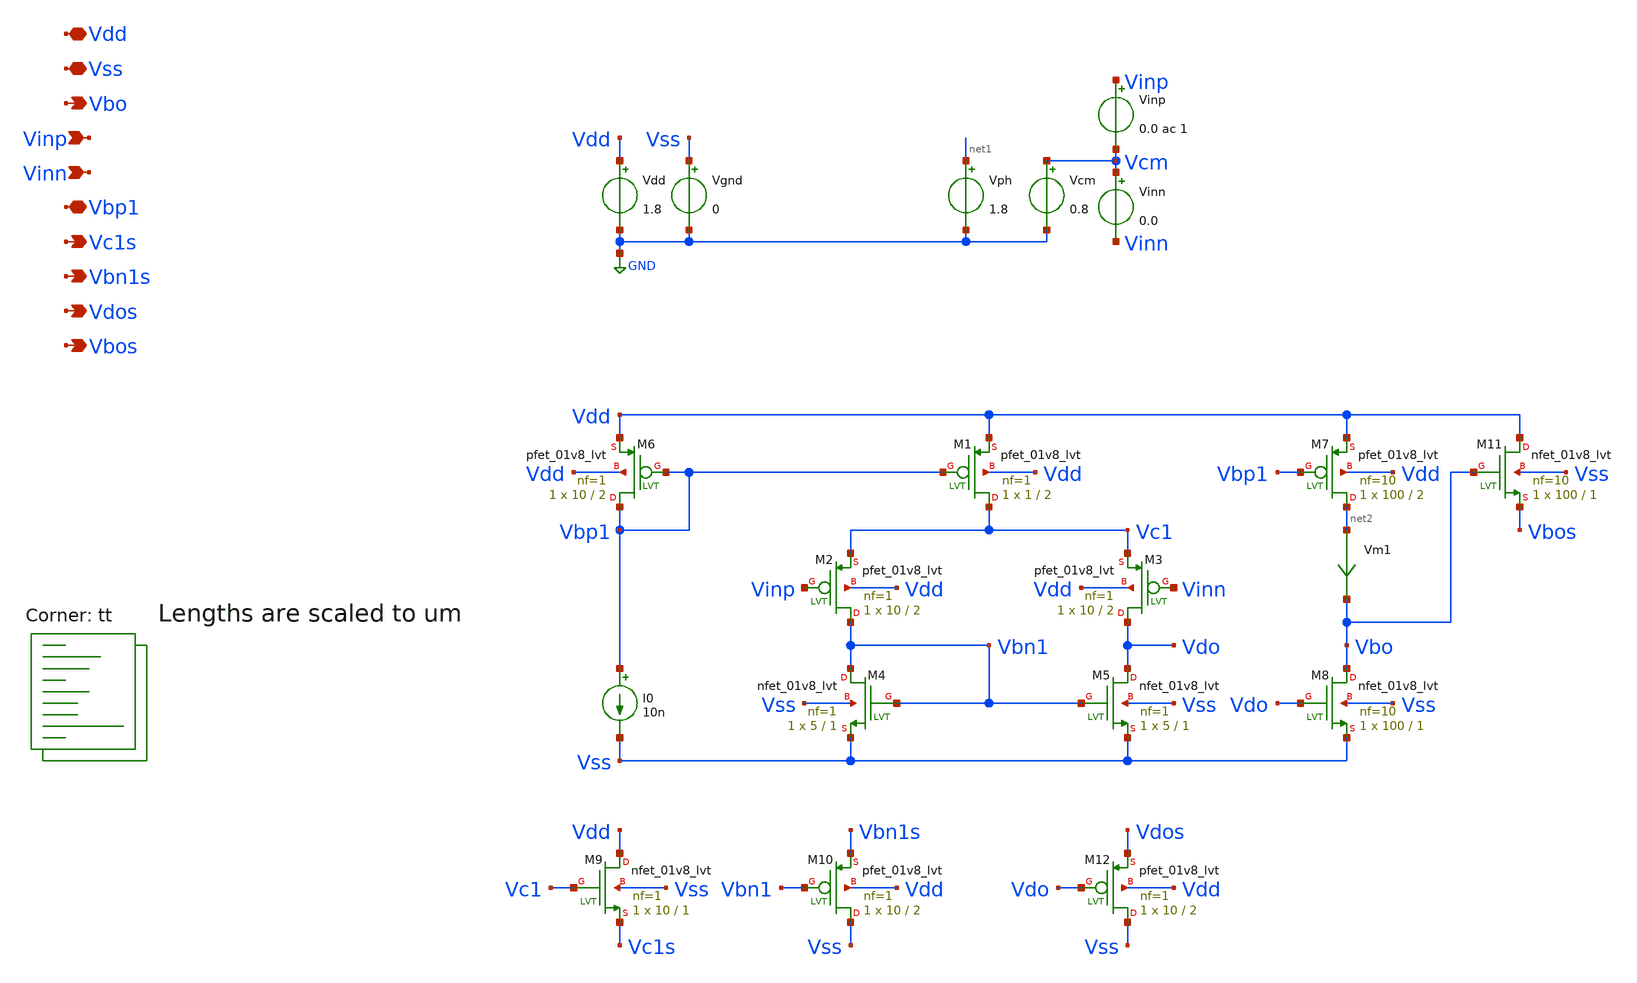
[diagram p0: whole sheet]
** sch_path: ic/CntDiffAmp/Schematic/CntDiffAmp0.sch
**.subckt CntDiffAmp0 Vinp Vbo Vinn Vdd Vss Vbp1 Vc1s Vbn1s Vdos Vbos
*.ipin Vinp
*.opin Vbo
*.ipin Vinn
*.iopin Vdd
*.iopin Vss
*.iopin Vbp1
*.opin Vc1s
*.opin Vbn1s
*.opin Vdos
*.opin Vbos
XM5 Vdo Vbn1 Vss Vss sky130_fd_pr__nfet_01v8_lvt L=1 W=5 nf=1 ad='int((nf+1)/2) * W/nf * 0.29' as='int((nf+2)/2) * W/nf * 0.29'
+ pd='2*int((nf+1)/2) * (W/nf + 0.29)' ps='2*int((nf+2)/2) * (W/nf + 0.29)' nrd='0.29 / W' nrs='0.29 / W'
+ sa=0 sb=0 sd=0 mult=1 m=1
XM4 Vbn1 Vbn1 Vss Vss sky130_fd_pr__nfet_01v8_lvt L=1 W=5 nf=1 ad='int((nf+1)/2) * W/nf * 0.29' as='int((nf+2)/2) * W/nf * 0.29'
+ pd='2*int((nf+1)/2) * (W/nf + 0.29)' ps='2*int((nf+2)/2) * (W/nf + 0.29)' nrd='0.29 / W' nrs='0.29 / W'
+ sa=0 sb=0 sd=0 mult=1 m=1
I0 Vbp1 Vss 10n
Vdd Vdd GND 1.8
Vgnd Vss GND 0
Vinp Vinp Vcm 0.0 ac 1
Vinn Vcm Vinn 0.0
Vph net1 GND 1.8
Vcm Vcm GND 0.8
XM1 Vc1 Vbp1 Vdd Vdd sky130_fd_pr__pfet_01v8_lvt L=2 W=1 nf=1 ad='int((nf+1)/2) * W/nf * 0.29' as='int((nf+2)/2) * W/nf * 0.29'
+ pd='2*int((nf+1)/2) * (W/nf + 0.29)' ps='2*int((nf+2)/2) * (W/nf + 0.29)' nrd='0.29 / W' nrs='0.29 / W'
+ sa=0 sb=0 sd=0 mult=1 m=1
XM6 Vbp1 Vbp1 Vdd Vdd sky130_fd_pr__pfet_01v8_lvt L=2 W=10 nf=1 ad='int((nf+1)/2) * W/nf * 0.29' as='int((nf+2)/2) * W/nf * 0.29'
+ pd='2*int((nf+1)/2) * (W/nf + 0.29)' ps='2*int((nf+2)/2) * (W/nf + 0.29)' nrd='0.29 / W' nrs='0.29 / W'
+ sa=0 sb=0 sd=0 mult=1 m=1
XM2 Vbn1 Vinp Vc1 Vdd sky130_fd_pr__pfet_01v8_lvt L=2 W=10 nf=1 ad='int((nf+1)/2) * W/nf * 0.29' as='int((nf+2)/2) * W/nf * 0.29'
+ pd='2*int((nf+1)/2) * (W/nf + 0.29)' ps='2*int((nf+2)/2) * (W/nf + 0.29)' nrd='0.29 / W' nrs='0.29 / W'
+ sa=0 sb=0 sd=0 mult=1 m=1
XM3 Vdo Vinn Vc1 Vdd sky130_fd_pr__pfet_01v8_lvt L=2 W=10 nf=1 ad='int((nf+1)/2) * W/nf * 0.29' as='int((nf+2)/2) * W/nf * 0.29'
+ pd='2*int((nf+1)/2) * (W/nf + 0.29)' ps='2*int((nf+2)/2) * (W/nf + 0.29)' nrd='0.29 / W' nrs='0.29 / W'
+ sa=0 sb=0 sd=0 mult=1 m=1
XM7 net2 Vbp1 Vdd Vdd sky130_fd_pr__pfet_01v8_lvt L=2 W=100 nf=10 ad='int((nf+1)/2) * W/nf * 0.29' as='int((nf+2)/2) * W/nf * 0.29'
+ pd='2*int((nf+1)/2) * (W/nf + 0.29)' ps='2*int((nf+2)/2) * (W/nf + 0.29)' nrd='0.29 / W' nrs='0.29 / W'
+ sa=0 sb=0 sd=0 mult=1 m=1
XM8 Vbo Vdo Vss Vss sky130_fd_pr__nfet_01v8_lvt L=1 W=100 nf=10 ad='int((nf+1)/2) * W/nf * 0.29' as='int((nf+2)/2) * W/nf * 0.29'
+ pd='2*int((nf+1)/2) * (W/nf + 0.29)' ps='2*int((nf+2)/2) * (W/nf + 0.29)' nrd='0.29 / W' nrs='0.29 / W'
+ sa=0 sb=0 sd=0 mult=1 m=1
Vm1 net2 Vbo 0
.save i(vm1)
XM9 Vdd Vc1 Vc1s Vss sky130_fd_pr__nfet_01v8_lvt L=1 W=10 nf=1 ad='int((nf+1)/2) * W/nf * 0.29' as='int((nf+2)/2) * W/nf * 0.29'
+ pd='2*int((nf+1)/2) * (W/nf + 0.29)' ps='2*int((nf+2)/2) * (W/nf + 0.29)' nrd='0.29 / W' nrs='0.29 / W'
+ sa=0 sb=0 sd=0 mult=1 m=1
XM10 Vss Vbn1 Vbn1s Vdd sky130_fd_pr__pfet_01v8_lvt L=2 W=10 nf=1 ad='int((nf+1)/2) * W/nf * 0.29' as='int((nf+2)/2) * W/nf * 0.29'
+ pd='2*int((nf+1)/2) * (W/nf + 0.29)' ps='2*int((nf+2)/2) * (W/nf + 0.29)' nrd='0.29 / W' nrs='0.29 / W'
+ sa=0 sb=0 sd=0 mult=1 m=1
XM11 Vdd Vbo Vbos Vss sky130_fd_pr__nfet_01v8_lvt L=1 W=100 nf=10 ad='int((nf+1)/2) * W/nf * 0.29' as='int((nf+2)/2) * W/nf * 0.29'
+ pd='2*int((nf+1)/2) * (W/nf + 0.29)' ps='2*int((nf+2)/2) * (W/nf + 0.29)' nrd='0.29 / W' nrs='0.29 / W'
+ sa=0 sb=0 sd=0 mult=1 m=1
XM12 Vss Vdo Vdos Vdd sky130_fd_pr__pfet_01v8_lvt L=2 W=10 nf=1 ad='int((nf+1)/2) * W/nf * 0.29' as='int((nf+2)/2) * W/nf * 0.29'
+ pd='2*int((nf+1)/2) * (W/nf + 0.29)' ps='2*int((nf+2)/2) * (W/nf + 0.29)' nrd='0.29 / W' nrs='0.29 / W'
+ sa=0 sb=0 sd=0 mult=1 m=1
**** begin user architecture code
.lib $::SKYWATER_MODELS/sky130.lib.spice tt

* this option enables mos model bin
* selection based on W/NF instead of W
.option wnflag=1
.option savecurrents acct abstol=1e-15
*reltol=1e-6
*gmin=1e-15

.control
save all
save @m.xm1.msky130_fd_pr__pfet_01v8_lvt[gm]
save @m.xm1.msky130_fd_pr__pfet_01v8_lvt[vth]
save @m.xm1.msky130_fd_pr__pfet_01v8_lvt[vdsat]
save @m.xm2.msky130_fd_pr__pfet_01v8_lvt[gm]
save @m.xm2.msky130_fd_pr__pfet_01v8_lvt[vth]
save @m.xm2.msky130_fd_pr__pfet_01v8_lvt[vdsat]
save @m.xm4.msky130_fd_pr__nfet_01v8_lvt[gm]
save @m.xm4.msky130_fd_pr__nfet_01v8_lvt[vth]
save @m.xm4.msky130_fd_pr__nfet_01v8_lvt[vdsat]

op
write CntDiffAmp0.raw

dc Vcm 0.0 1.8 0.01
plot v(Vdo), v(Vbo) vs v(Vcm)
plot v(Vc1), v(Vbp1), v(Vbn1) vs v(Vcm)
plot @m.xm2.msky130_fd_pr__pfet_01v8_lvt[gm], @m.xm4.msky130_fd_pr__nfet_01v8_lvt[gm] vs V(Vcm)

dc Vinp -1.0 1.0 0.01
plot v(Vdo), v(Vbo) vs v(Vinp)

set appendwrite
write CntDiffAmp0.raw

ac dec 10 1 1e9
plot vdb(Vdo), vdb(Vbo)

write CntDiffAmp0.raw
.endc




** CntFET model
.subckt cntnfet_a d g s b
.param l=1 w=0.01 mult=1
mcntnfet_a d g s b cntnfet l={l} w={w}
* BSIM4 model
.model cntnfet nmos  level=54 version=4.8.2  toxe=7e-9
.ends cntnfet_a

.subckt cntpfet_a d g s b
.param l=1 w=0.01 mult=1
mcntpfet_a d g s b cntpfet l={l} w={w}
* BSIM4 model
.model cntpfet pmos  level=54 version=4.8.2  toxe=100e-9 U0=1.09e-4 VTH0=-2.02
.ends cntnfet_a

.model cntnfet_b nmos level=54 version=4.8.2 toxe=5e-9
.model cntpfet_b nmos level=54 version=4.8.2 toxe=5e-9


**** end user architecture code
**.ends
.GLOBAL GND
.end
